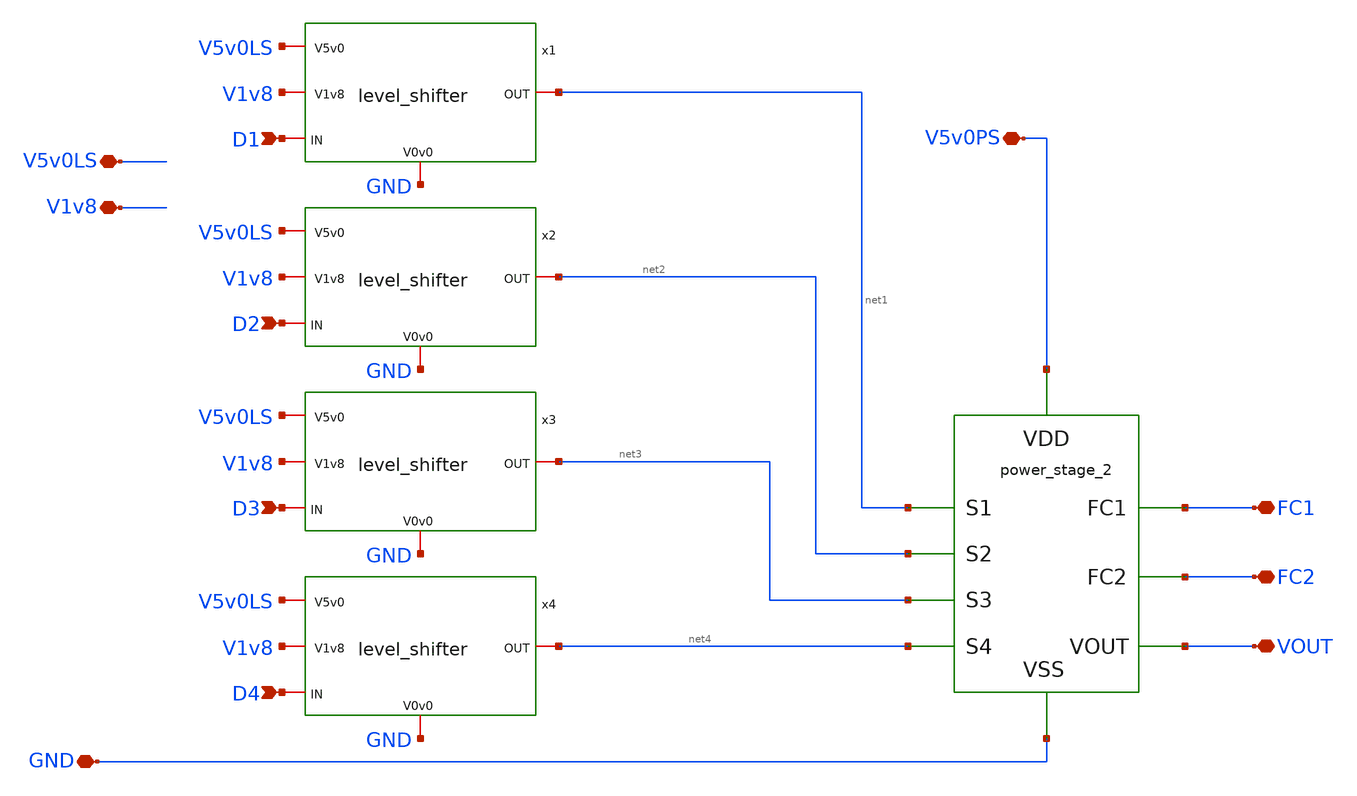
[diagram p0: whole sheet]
** sch_path: xschem/converter_2.sch
**.subckt converter_2 V5v0PS D1 D2 D3 D4 V1v8 GND V5v0LS FC1 FC2 VOUT
*.iopin V5v0PS
*.ipin D1
*.ipin D2
*.ipin D3
*.ipin D4
*.iopin V1v8
*.iopin GND
*.iopin V5v0LS
*.iopin FC1
*.iopin FC2
*.iopin VOUT
x4 V5v0LS V1v8 net4 D4 GND level_shifter
x3 V5v0LS V1v8 net3 D3 GND level_shifter
x2 V5v0LS V1v8 net2 D2 GND level_shifter
x1 V5v0LS V1v8 net1 D1 GND level_shifter
X5 net1 net2 net3 net4 FC1 FC2 VOUT V5v0PS GND power_stage_2
**.ends

* expanding   symbol:  level_shifter.sym # of pins=5
** sym_path: xschem/level_shifter.sym
** sch_path: xschem/level_shifter.sch
.subckt level_shifter V5v0 V1v8 OUT IN V0v0
*.ipin IN
*.iopin V1v8
*.iopin V5v0
*.opin OUT
*.iopin V0v0
XM11 net1 IN V1v8 V1v8 sky130_fd_pr__pfet_01v8 L=0.15 W=1 nf=1 ad='int((nf+1)/2) * W/nf * 0.29' as='int((nf+2)/2) * W/nf * 0.29'
+ pd='2*int((nf+1)/2) * (W/nf + 0.29)' ps='2*int((nf+2)/2) * (W/nf + 0.29)' nrd='0.29 / W' nrs='0.29 / W'
+ sa=0 sb=0 sd=0 mult=5 m=5
XM12 net1 IN V0v0 V0v0 sky130_fd_pr__nfet_01v8 L=0.15 W=1 nf=1 ad='int((nf+1)/2) * W/nf * 0.29' as='int((nf+2)/2) * W/nf * 0.29'
+ pd='2*int((nf+1)/2) * (W/nf + 0.29)' ps='2*int((nf+2)/2) * (W/nf + 0.29)' nrd='0.29 / W' nrs='0.29 / W'
+ sa=0 sb=0 sd=0 mult=5 m=5
XM15 net2 net3 V5v0 V5v0 sky130_fd_pr__pfet_g5v0d10v5 L=0.5 W=2 nf=1 ad='int((nf+1)/2) * W/nf * 0.29'
+ as='int((nf+2)/2) * W/nf * 0.29' pd='2*int((nf+1)/2) * (W/nf + 0.29)' ps='2*int((nf+2)/2) * (W/nf + 0.29)'
+ nrd='0.29 / W' nrs='0.29 / W' sa=0 sb=0 sd=0 mult=1 m=1
XM14 net3 net2 V5v0 V5v0 sky130_fd_pr__pfet_g5v0d10v5 L=0.5 W=2 nf=1 ad='int((nf+1)/2) * W/nf * 0.29'
+ as='int((nf+2)/2) * W/nf * 0.29' pd='2*int((nf+1)/2) * (W/nf + 0.29)' ps='2*int((nf+2)/2) * (W/nf + 0.29)'
+ nrd='0.29 / W' nrs='0.29 / W' sa=0 sb=0 sd=0 mult=1 m=1
XM16 net4 net2 V5v0 V5v0 sky130_fd_pr__pfet_g5v0d10v5 L=0.5 W=10 nf=1 ad='int((nf+1)/2) * W/nf * 0.29'
+ as='int((nf+2)/2) * W/nf * 0.29' pd='2*int((nf+1)/2) * (W/nf + 0.29)' ps='2*int((nf+2)/2) * (W/nf + 0.29)'
+ nrd='0.29 / W' nrs='0.29 / W' sa=0 sb=0 sd=0 mult=10 m=10
XM18 net2 net1 V0v0 V0v0 sky130_fd_pr__nfet_g5v0d10v5 L=0.5 W=4 nf=1 ad='int((nf+1)/2) * W/nf * 0.29'
+ as='int((nf+2)/2) * W/nf * 0.29' pd='2*int((nf+1)/2) * (W/nf + 0.29)' ps='2*int((nf+2)/2) * (W/nf + 0.29)'
+ nrd='0.29 / W' nrs='0.29 / W' sa=0 sb=0 sd=0 mult=3 m=3
XM13 net3 IN V0v0 V0v0 sky130_fd_pr__nfet_g5v0d10v5 L=0.5 W=4 nf=1 ad='int((nf+1)/2) * W/nf * 0.29' as='int((nf+2)/2) * W/nf * 0.29'
+ pd='2*int((nf+1)/2) * (W/nf + 0.29)' ps='2*int((nf+2)/2) * (W/nf + 0.29)' nrd='0.29 / W' nrs='0.29 / W'
+ sa=0 sb=0 sd=0 mult=3 m=3
XM17 net4 IN V0v0 V0v0 sky130_fd_pr__nfet_g5v0d10v5 L=0.5 W=10 nf=1 ad='int((nf+1)/2) * W/nf * 0.29'
+ as='int((nf+2)/2) * W/nf * 0.29' pd='2*int((nf+1)/2) * (W/nf + 0.29)' ps='2*int((nf+2)/2) * (W/nf + 0.29)'
+ nrd='0.29 / W' nrs='0.29 / W' sa=0 sb=0 sd=0 mult=10 m=10
XM7 OUT net4 V5v0 V5v0 sky130_fd_pr__pfet_g5v0d10v5 L=0.5 W=20 nf=1 ad='int((nf+1)/2) * W/nf * 0.29'
+ as='int((nf+2)/2) * W/nf * 0.29' pd='2*int((nf+1)/2) * (W/nf + 0.29)' ps='2*int((nf+2)/2) * (W/nf + 0.29)'
+ nrd='0.29 / W' nrs='0.29 / W' sa=0 sb=0 sd=0 mult=20 m=20
XM10 OUT net4 V0v0 V0v0 sky130_fd_pr__nfet_g5v0d10v5 L=0.5 W=20 nf=1 ad='int((nf+1)/2) * W/nf * 0.29'
+ as='int((nf+2)/2) * W/nf * 0.29' pd='2*int((nf+1)/2) * (W/nf + 0.29)' ps='2*int((nf+2)/2) * (W/nf + 0.29)'
+ nrd='0.29 / W' nrs='0.29 / W' sa=0 sb=0 sd=0 mult=20 m=20
.ends


* expanding   symbol:  power_stage_2.sym # of pins=9
** sym_path: xschem/power_stage_2.sym
** sch_path: xschem/power_stage_2.sch
.subckt power_stage_2 S1 S2 S3 S4 FC1 FC2 VOUT VDD VSS
*.iopin VDD
*.ipin S1
*.ipin S2
*.iopin VOUT
*.ipin S3
*.ipin S4
*.iopin VSS
*.iopin FC1
*.iopin FC2
XM2 VOUT S2 FC1 FC1 sky130_fd_pr__pfet_g5v0d10v5 L=0.5 W=4.38 nf=1 ad='int((nf+1)/2) * W/nf * 0.29' as='int((nf+2)/2) * W/nf * 0.29'
+ pd='2*int((nf+1)/2) * (W/nf + 0.29)' ps='2*int((nf+2)/2) * (W/nf + 0.29)' nrd='0.29 / W' nrs='0.29 / W'
+ sa=0 sb=0 sd=0 mult=1300 m=1300
XM1 FC1 S1 VDD VDD sky130_fd_pr__pfet_g5v0d10v5 L=0.5 W=4.38 nf=1 ad='int((nf+1)/2) * W/nf * 0.29' as='int((nf+2)/2) * W/nf * 0.29'
+ pd='2*int((nf+1)/2) * (W/nf + 0.29)' ps='2*int((nf+2)/2) * (W/nf + 0.29)' nrd='0.29 / W' nrs='0.29 / W'
+ sa=0 sb=0 sd=0 mult=1300 m=1300
XM3 VOUT S3 FC2 FC2 sky130_fd_pr__nfet_g5v0d10v5 L=0.5 W=4.38 nf=1 ad='int((nf+1)/2) * W/nf * 0.29' as='int((nf+2)/2) * W/nf * 0.29'
+ pd='2*int((nf+1)/2) * (W/nf + 0.29)' ps='2*int((nf+2)/2) * (W/nf + 0.29)' nrd='0.29 / W' nrs='0.29 / W'
+ sa=0 sb=0 sd=0 mult=364 m=364
XM4 FC2 S4 VSS VSS sky130_fd_pr__nfet_g5v0d10v5 L=0.5 W=4.38 nf=1 ad='int((nf+1)/2) * W/nf * 0.29' as='int((nf+2)/2) * W/nf * 0.29'
+ pd='2*int((nf+1)/2) * (W/nf + 0.29)' ps='2*int((nf+2)/2) * (W/nf + 0.29)' nrd='0.29 / W' nrs='0.29 / W'
+ sa=0 sb=0 sd=0 mult=364 m=364
.ends

.end
